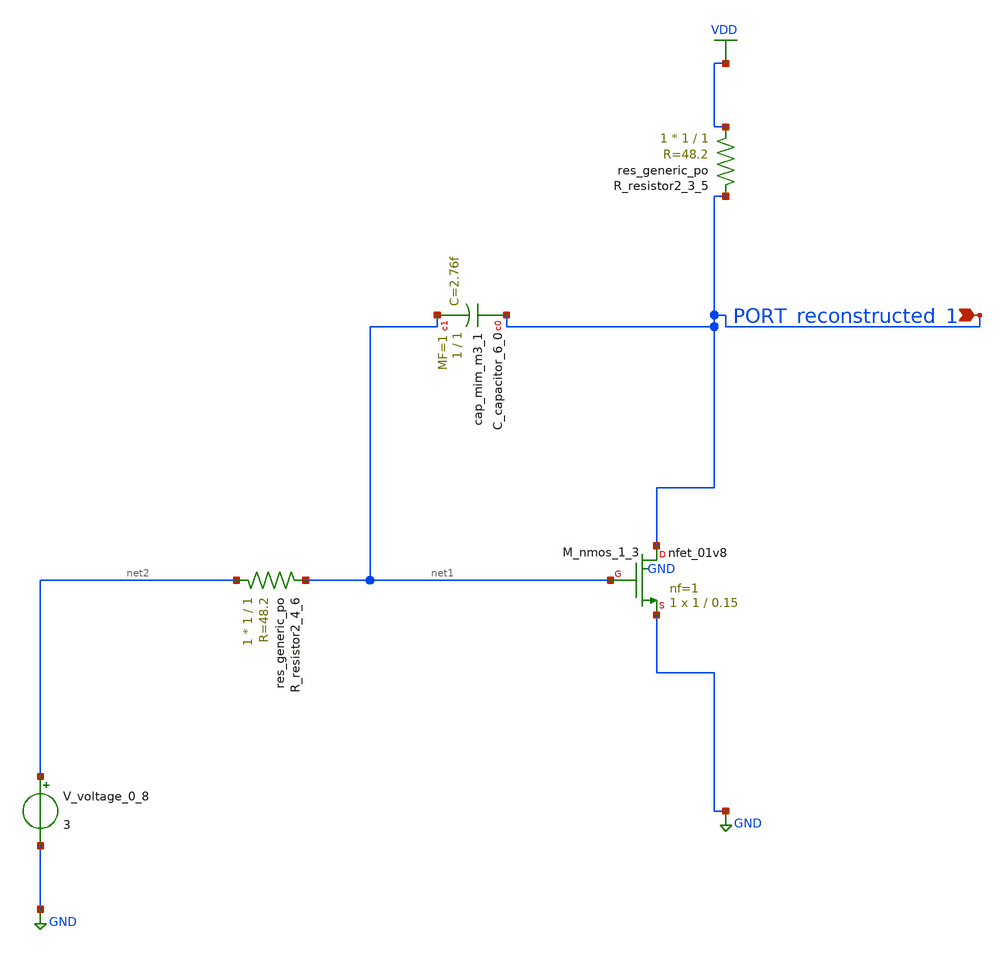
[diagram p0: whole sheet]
** sch_path: schematics/AMSNet/398.sch
**.subckt 398 PORT_reconstructed_1
*.ipin PORT_reconstructed_1
XC_capacitor_6_0 PORT_reconstructed_1 net1 sky130_fd_pr__cap_mim_m3_1 W=1 L=1 MF=1 m=1
XM_nmos_1_3 PORT_reconstructed_1 net1 GND GND sky130_fd_pr__nfet_01v8 L=0.15 W=1 nf=1 ad='int((1 + 1)/2) * 1 / 1 * 0.29'
+ as='int((1 + 2)/2) * 1 / 1 * 0.29' pd='2*int((1 + 1)/2) * (1 / 1 + 0.29)' ps='2*int((1 + 2)/2) * (1 / 1 + 0.29)'
+ nrd='0.29 / 1 ' nrs='0.29 / 1 ' sa=0 sb=0 sd=0 mult=1 m=1
XR_resistor2_3_5 VDD PORT_reconstructed_1 sky130_fd_pr__res_generic_po W=1 L=1 m=1
XR_resistor2_4_6 net2 net1 sky130_fd_pr__res_generic_po W=1 L=1 m=1
V_voltage_0_8 net2 GND 3
**.ends
.GLOBAL GND
.GLOBAL VDD
.end
